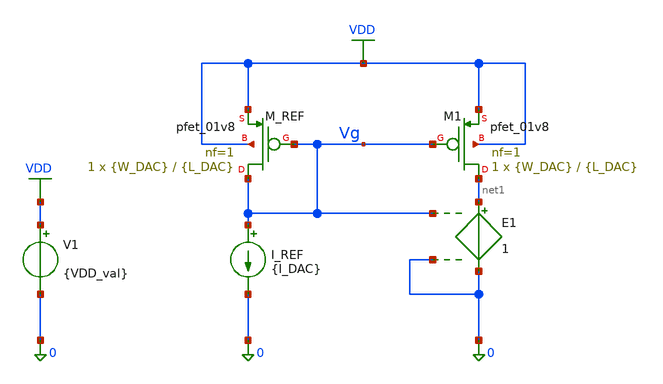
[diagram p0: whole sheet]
** sch_path: designs_backup/designs/lab2/CURRENT_SOURCE.sch
**.subckt CURRENT_SOURCE
I_REF Vg 0 {I_DAC}
E1 net1 0 Vg 0 1
V1 VDD 0 {VDD_val}
XM1 net1 Vg VDD VDD sky130_fd_pr__pfet_01v8 L={L_DAC} W={W_DAC} nf=1 ad='int((1 + 1)/2) * {W_DAC} / 1 * 0.29'
+ as='int((1 + 2)/2) * {W_DAC} / 1 * 0.29' pd='2*int((1 + 1)/2) * ({W_DAC} / 1 + 0.29)' ps='2*int((1 + 2)/2) * ({W_DAC} / 1 + 0.29)'
+ nrd='0.29 / {W_DAC} ' nrs='0.29 / {W_DAC} ' sa=0 sb=0 sd=0 mult=1 m=1
XM_REF Vg Vg VDD VDD sky130_fd_pr__pfet_01v8 L={L_DAC} W={W_DAC} nf=1 ad='int((1 + 1)/2) * {W_DAC} / 1 * 0.29'
+ as='int((1 + 2)/2) * {W_DAC} / 1 * 0.29' pd='2*int((1 + 1)/2) * ({W_DAC} / 1 + 0.29)' ps='2*int((1 + 2)/2) * ({W_DAC} / 1 + 0.29)'
+ nrd='0.29 / {W_DAC} ' nrs='0.29 / {W_DAC} ' sa=0 sb=0 sd=0 mult=1 m=1
**** begin user architecture code

** opencircuitdesign pdks install
.lib $::SKYWATER_MODELS/sky130.lib.spice tt

* force include MC files
.include "$::SKYWATER_MODELS/parameters/montecarlo.spice"
.include "$::SKYWATER_MODELS/parameters/critical.spice"

* force mismatch/process params
.param mc_mm_switch = 0
.param mc_pr_switch = 0

* disable pfet_ideal from mismatch/process
.subckt sky130_fd_pr__pfet_ideal D G S B W=0.42 L=0.15  nf=1 ad='int((1 + 1)/2) * {W} / 1 * 0.29' as='int((1 + 2)/2) * {W} / 1 * 0.29'
+  pd='2*int((1 + 1)/2) * ({W} / 1 + 0.29)' ps='2*int((1 + 2)/2) * ({W} / 1 + 0.29)'   nrd='0.29 / {W}'
+ nrs='0.29 / {W}' sa=0 sb=0 sd=0 mult=1
  .param mc_mm_switch=0
  .param mc_pr_switch=0
  XIDEAL D G S B sky130_fd_pr__pfet_01v8 W={W} L={L}
  + nf={nf} ad={ad} as={as} pd={pd} ps={ps}
  + nrd={nrd} nrs={nrs} sa={sa} sb={sb} sd={sd} mult={mult}
.ends



.param W_DAC = 0.42 L_DAC = 0.15
.param I_DAC = 100n
.param VDD_val = 1.8
.options savecurrents

.control
  * Clear M1 files
  shell mkdir -p /foss/designs/lab2/results/1.2
  shell rm -f /foss/designs/lab2/results/1.2/M1_Vgs_Vth.dat
  * I_REF current sweep
  foreach idac_val 100n 10u
    * W/L group sweep (indexed W/L groups)
    foreach case_idx 1 2 3
      if $case_idx = 1
        alterparam W_DAC = 0.42
        alterparam L_DAC = 0.15
      end
      if $case_idx = 2
        alterparam W_DAC = 5.0
        alterparam L_DAC = 3.5
      end
      if $case_idx = 3
        alterparam W_DAC = 3.5
        alterparam L_DAC = 5.0
      end
      alterparam I_DAC = $idac_val
      reset
      op
      set appendwrite
      * NOTE: The syntax for extracting model params depends on the exact instance name in the PDK.
      * Typically, for Xschem, this is @m.xm1.msky130_fd_pr__pfet_01v8[model_parameter]
      let scale = 1e6
      * scaled to um
      let W = @m.xm1.msky130_fd_pr__pfet_01v8[w]*scale
      let L = @m.xm1.msky130_fd_pr__pfet_01v8[l]*scale
      let vg_val = v(Vg)
      let vgs_val = @m.xm1.msky130_fd_pr__pfet_01v8[vgs]
      let vth_val = @m.xm1.msky130_fd_pr__pfet_01v8[vth]

      echo W/L= $&W / $&L [um] Idac= $idac_val [A] >> /foss/designs/lab2/results/1.2/M1_Vgs_Vth.dat
      echo Vg= $&vg_val Vgs= $&vgs_val Vth= $&vth_val >>
+ /foss/designs/lab2/results/1.2/M1_Vgs_Vth.dat
      echo >> /foss/designs/lab2/results/1.2/M1_Vgs_Vth.dat
    end
  end
.endc


**** end user architecture code
**.ends
.GLOBAL VDD
.end
